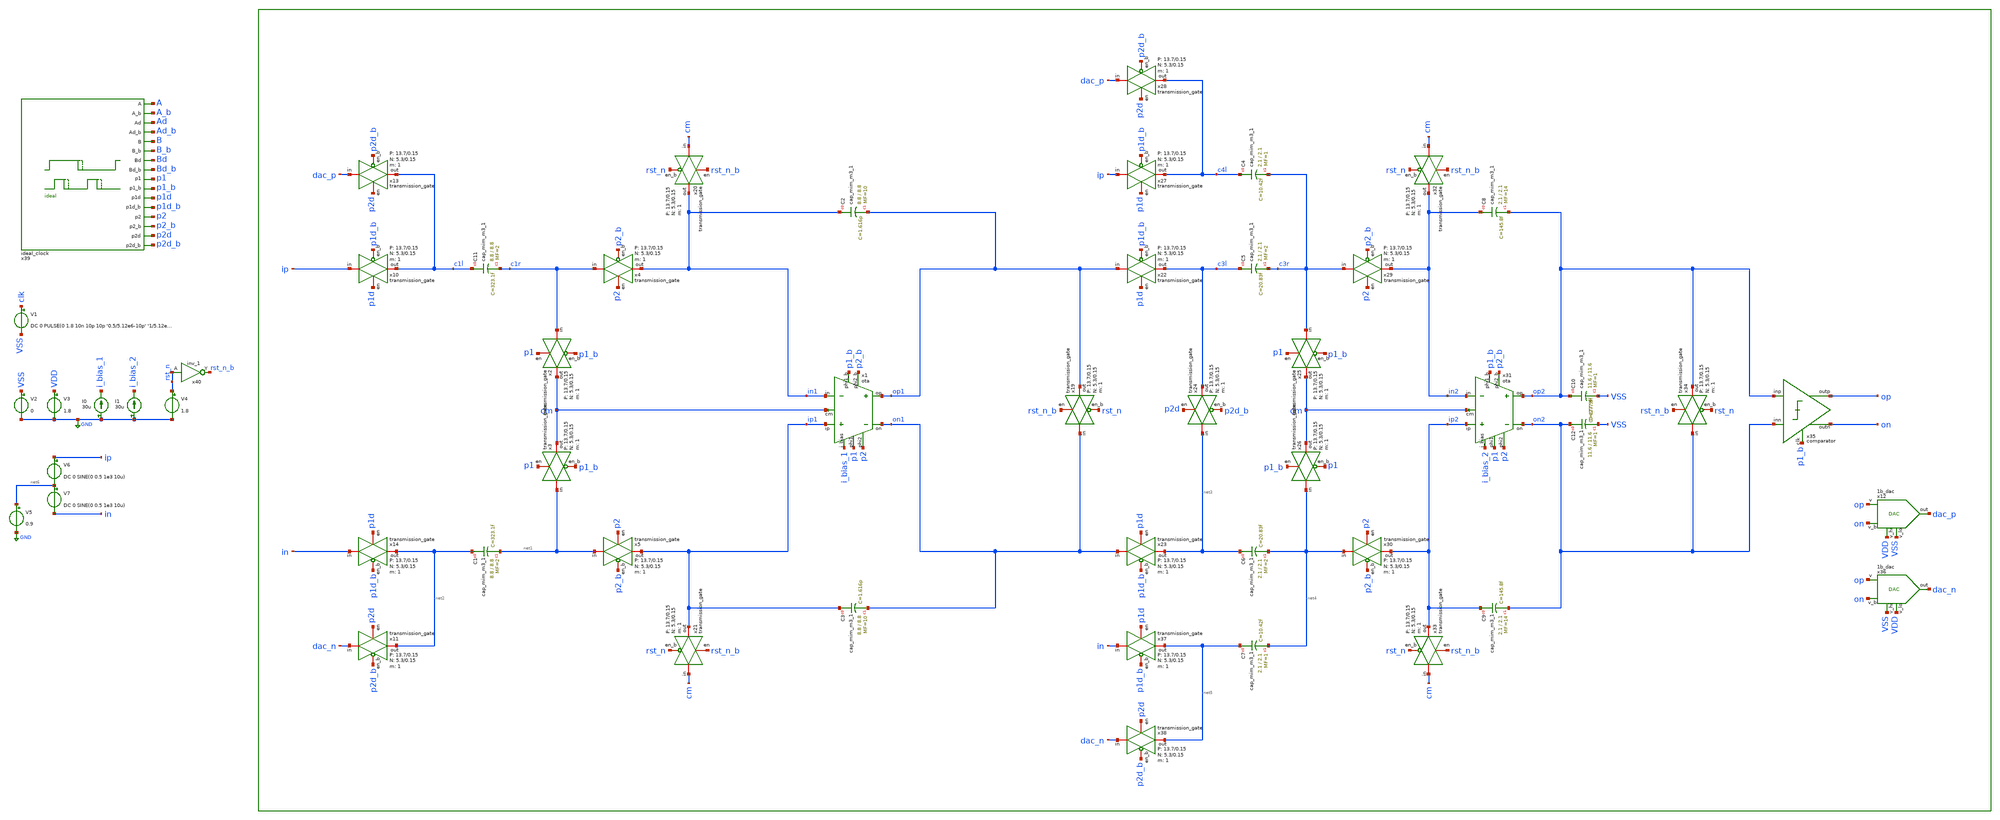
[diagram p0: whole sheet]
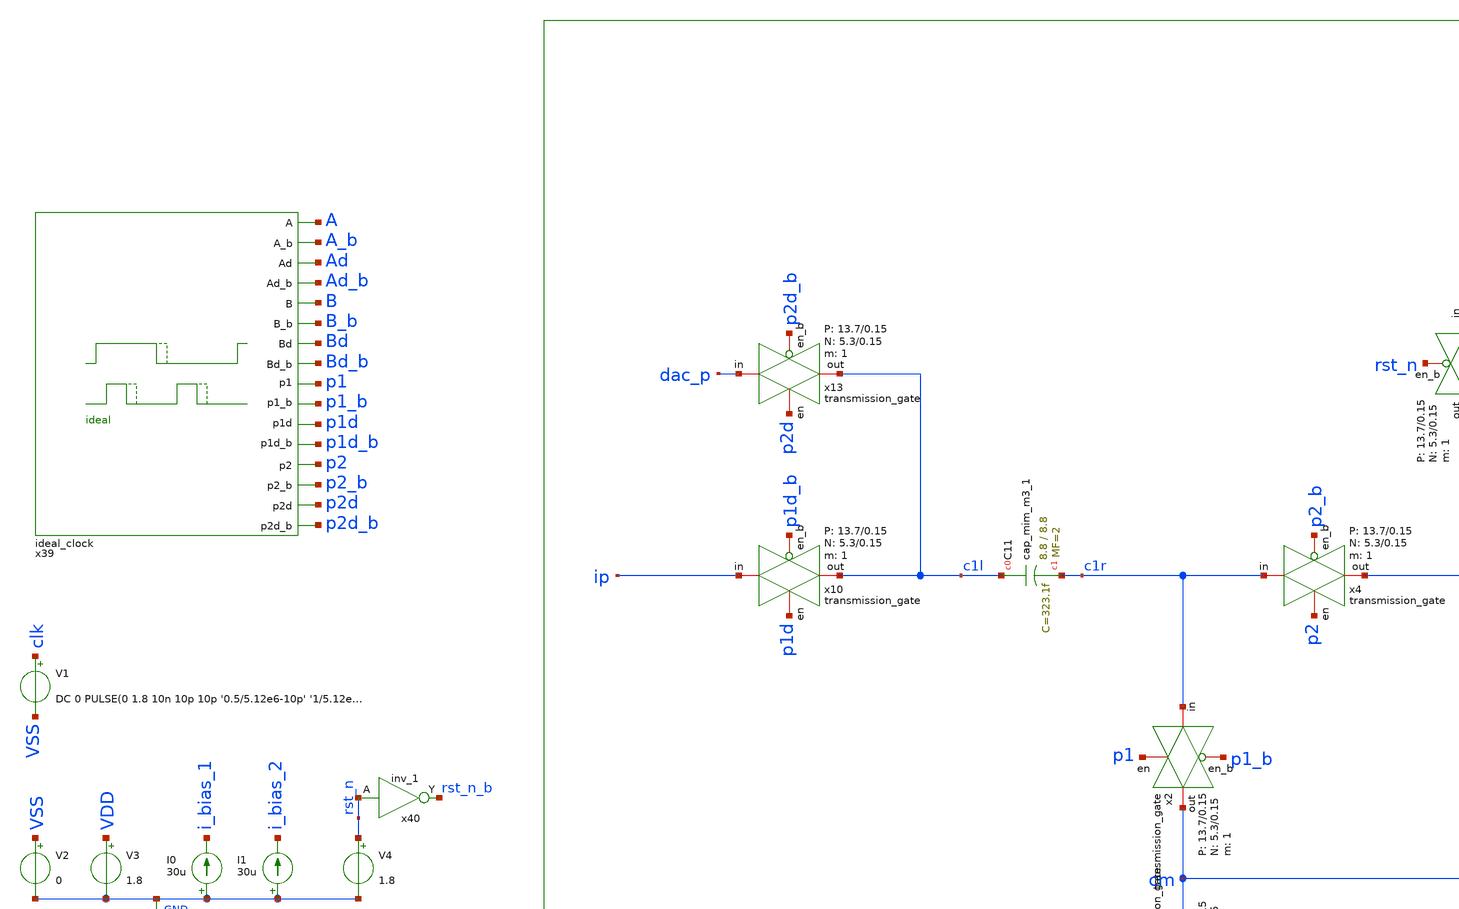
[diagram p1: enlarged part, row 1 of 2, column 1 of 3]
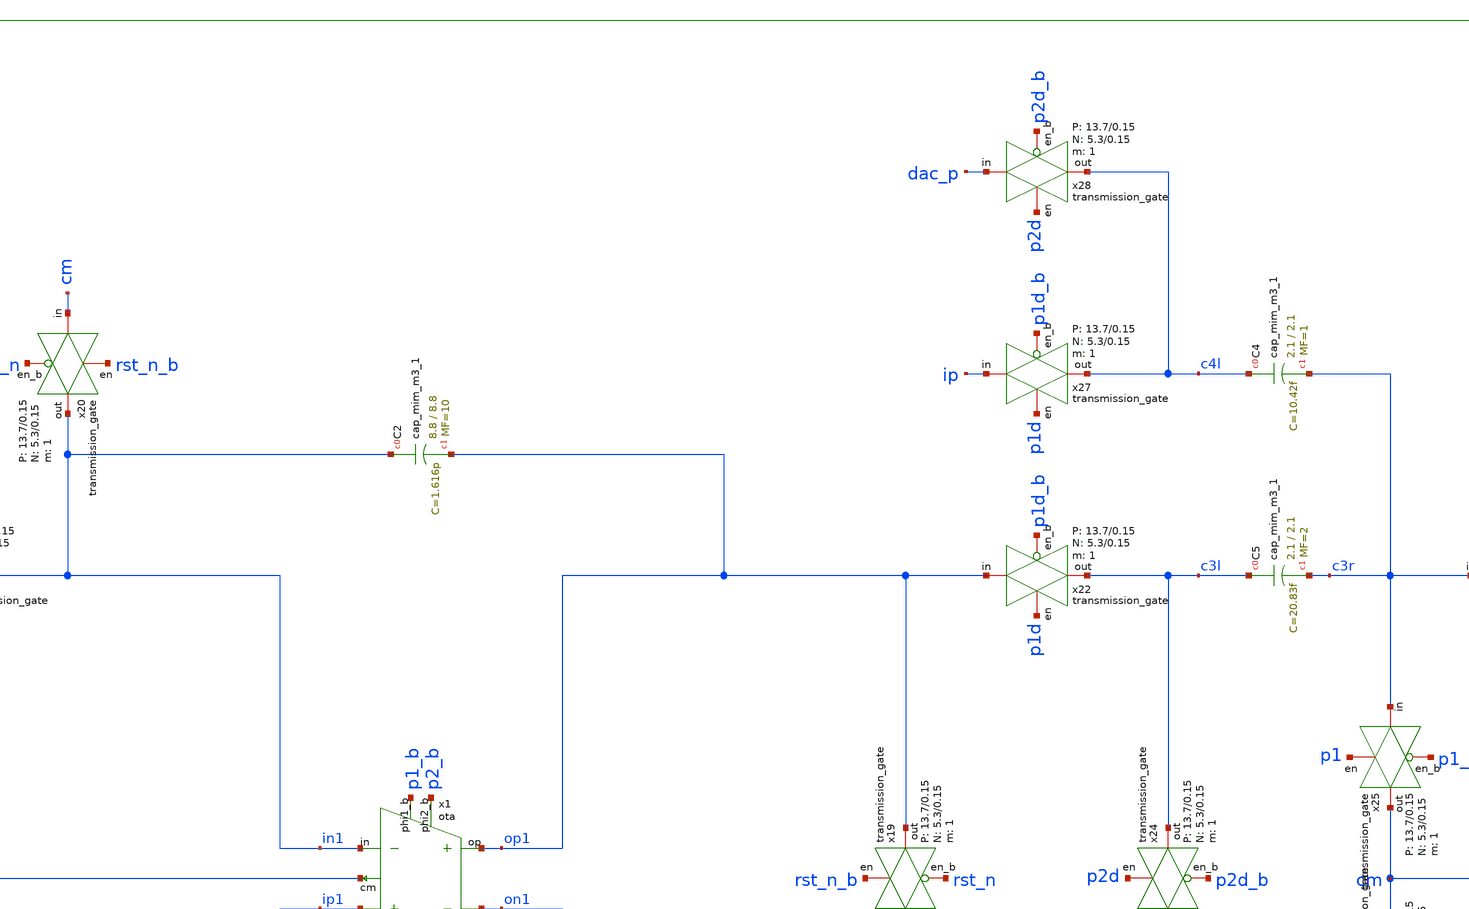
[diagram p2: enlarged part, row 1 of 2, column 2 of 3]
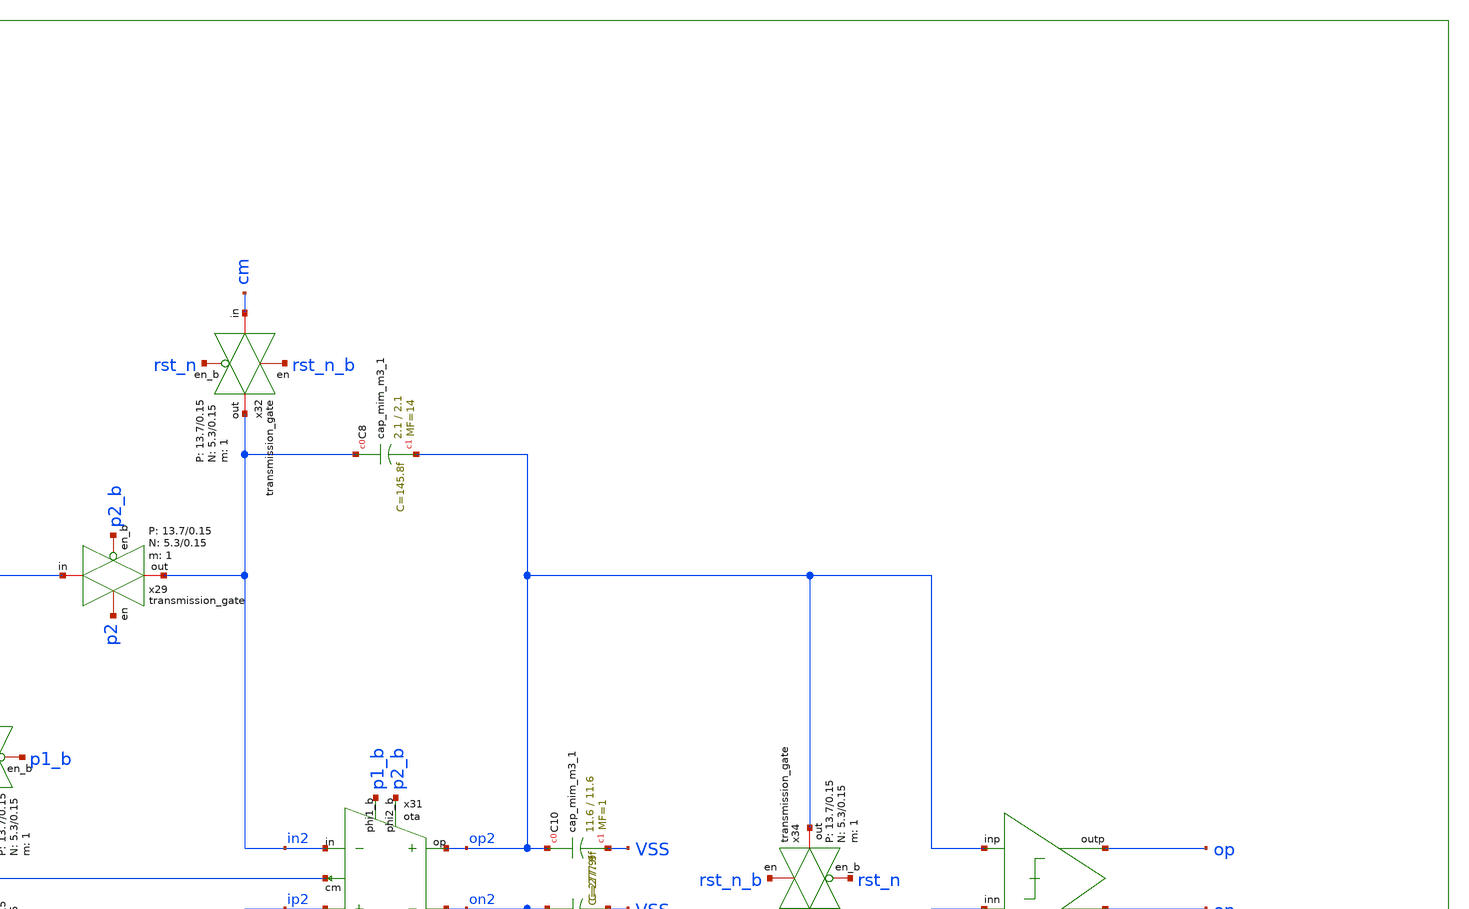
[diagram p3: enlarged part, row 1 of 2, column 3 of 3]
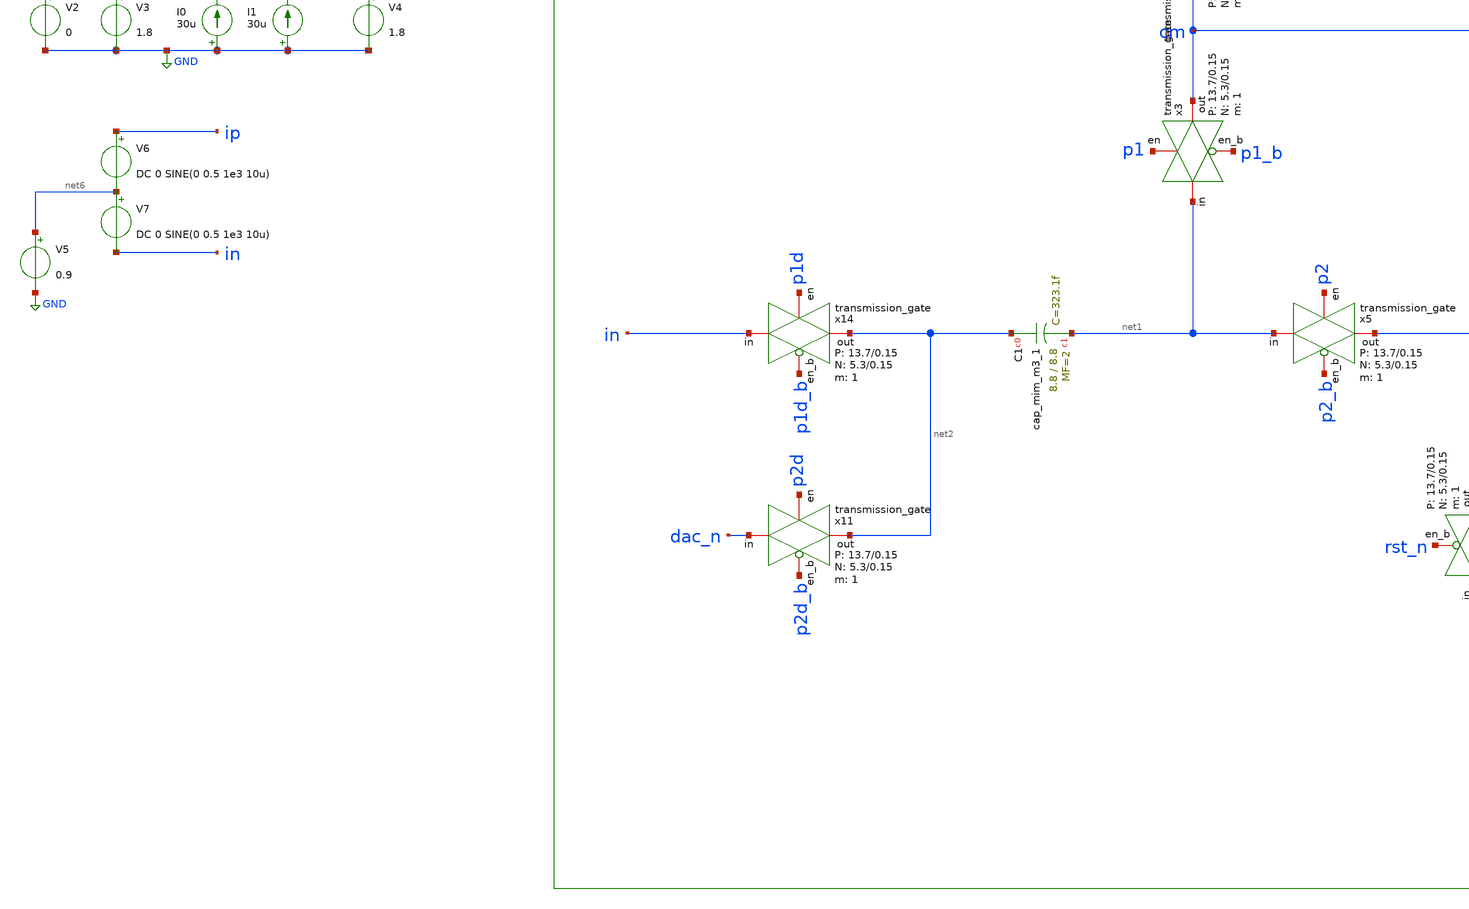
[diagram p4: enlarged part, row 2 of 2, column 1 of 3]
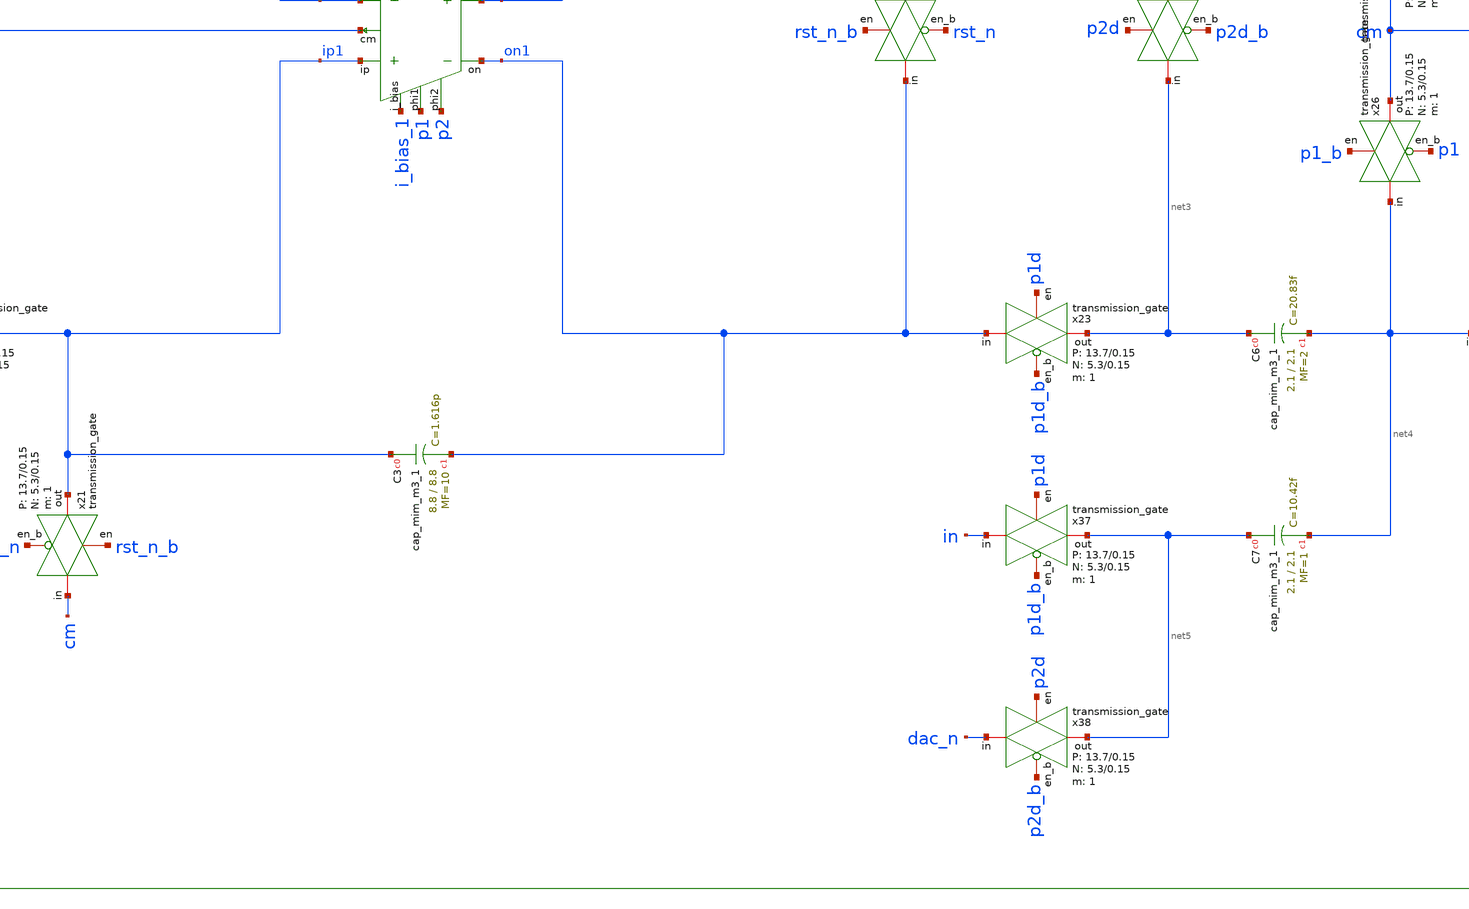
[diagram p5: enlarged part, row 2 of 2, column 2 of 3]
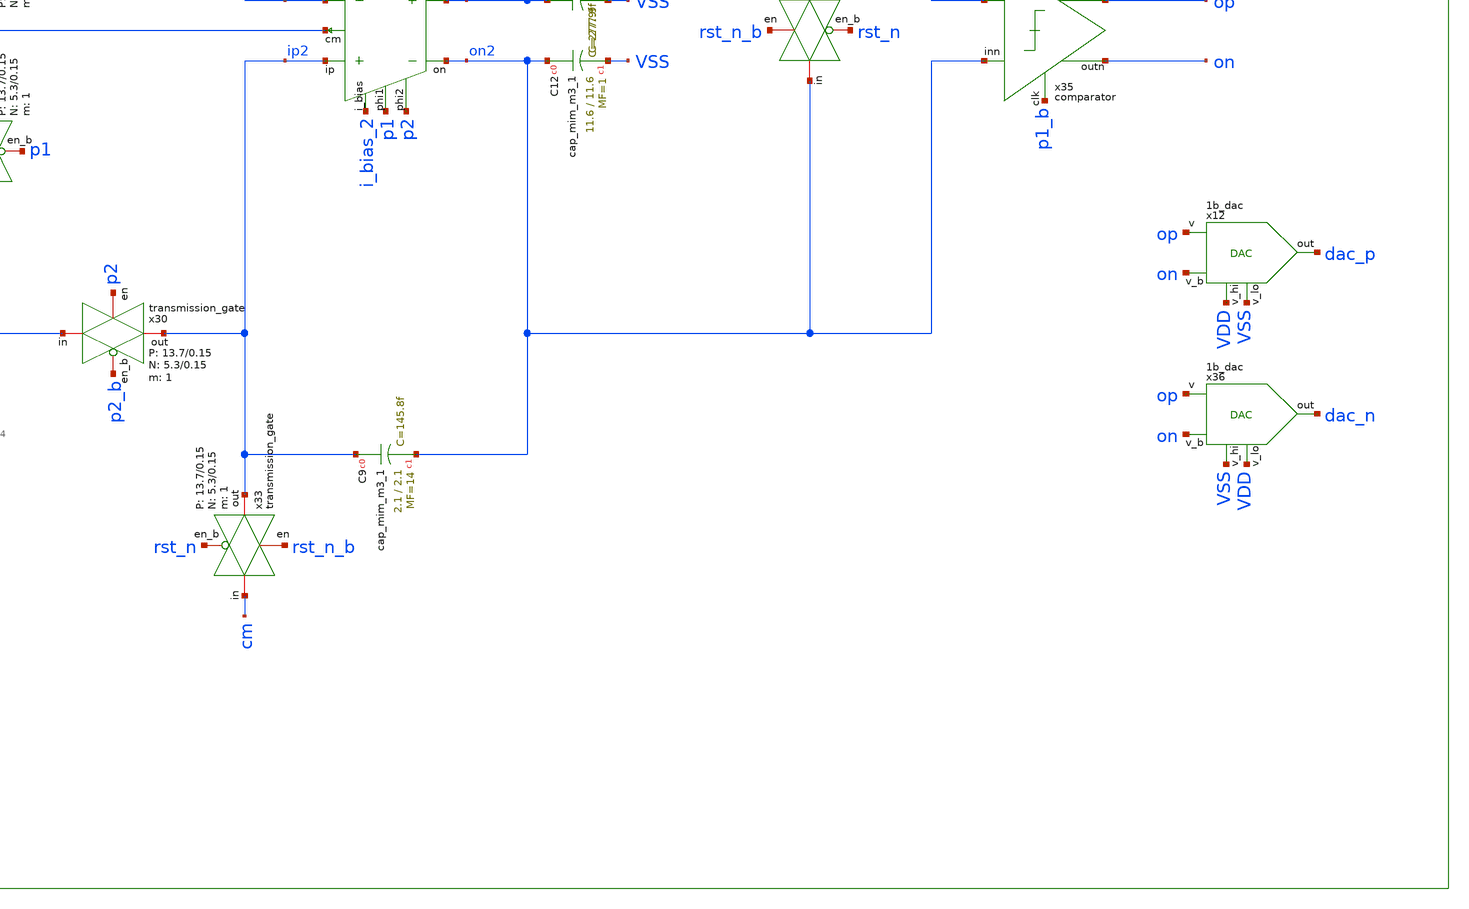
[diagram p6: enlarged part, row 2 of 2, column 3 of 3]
** sch_path: verification/schematic_sim/modulator_tb_ideal_clock_no_chopping.sch
**.subckt modulator_tb_ideal_clock_no_chopping
x1 i_bias_1 ip1 in1 p1 p1_b p2 p2_b op1 on1 cm 50 350 VDD VSS ota
x4 c1r in1 p2 p2_b VDD VSS 1 5.3 0.15 13.7 0.15 transmission_gate
x5 net1 ip1 p2 p2_b VDD VSS 1 5.3 0.15 13.7 0.15 transmission_gate
x2 c1r cm p1 p1_b VDD VSS 1 5.3 0.15 13.7 0.15 transmission_gate
x3 net1 cm p1 p1_b VDD VSS 1 5.3 0.15 13.7 0.15 transmission_gate
x10 ip c1l p1d p1d_b VDD VSS 1 5.3 0.15 13.7 0.15 transmission_gate
x11 dac_n net2 p2d p2d_b VDD VSS 1 5.3 0.15 13.7 0.15 transmission_gate
x12 VDD VSS op dac_p on VDD VSS 1b_dac
x13 dac_p c1l p2d p2d_b VDD VSS 1 5.3 0.15 13.7 0.15 transmission_gate
x14 in net2 p1d p1d_b VDD VSS 1 5.3 0.15 13.7 0.15 transmission_gate
x19 on1 op1 rst_n_b rst_n VDD VSS 1 5.3 0.15 13.7 0.15 transmission_gate
x20 cm in1 rst_n_b rst_n VDD VSS 1 5.3 0.15 13.7 0.15 transmission_gate
x21 cm ip1 rst_n_b rst_n VDD VSS 1 5.3 0.15 13.7 0.15 transmission_gate
x22 op1 c3l p1d p1d_b VDD VSS 1 5.3 0.15 13.7 0.15 transmission_gate
x23 on1 net3 p1d p1d_b VDD VSS 1 5.3 0.15 13.7 0.15 transmission_gate
x24 net3 c3l p2d p2d_b VDD VSS 1 5.3 0.15 13.7 0.15 transmission_gate
x25 c3r cm p1 p1_b VDD VSS 1 5.3 0.15 13.7 0.15 transmission_gate
x26 net4 cm p1_b p1 VDD VSS 1 5.3 0.15 13.7 0.15 transmission_gate
x27 ip c4l p1d p1d_b VDD VSS 1 5.3 0.15 13.7 0.15 transmission_gate
x28 dac_p c4l p2d p2d_b VDD VSS 1 5.3 0.15 13.7 0.15 transmission_gate
x29 c3r in2 p2 p2_b VDD VSS 1 5.3 0.15 13.7 0.15 transmission_gate
x30 net4 ip2 p2 p2_b VDD VSS 1 5.3 0.15 13.7 0.15 transmission_gate
x31 i_bias_2 ip2 in2 p1 p1_b p2 p2_b op2 on2 cm 50 350 VDD VSS ota
x32 cm in2 rst_n_b rst_n VDD VSS 1 5.3 0.15 13.7 0.15 transmission_gate
x33 cm ip2 rst_n_b rst_n VDD VSS 1 5.3 0.15 13.7 0.15 transmission_gate
x34 on2 op2 rst_n_b rst_n VDD VSS 1 5.3 0.15 13.7 0.15 transmission_gate
x35 op2 on2 op p1_b on VDD VSS comparator
x36 VSS VDD op dac_n on VDD VSS 1b_dac
x37 in net5 p1d p1d_b VDD VSS 1 5.3 0.15 13.7 0.15 transmission_gate
x38 dac_n net5 p2d p2d_b VDD VSS 1 5.3 0.15 13.7 0.15 transmission_gate
V1 clk VSS DC 0 PULSE(0 1.8 10n 10p 10p '0.5/5.12e6-10p' '1/5.12e6')
V2 VSS GND 0
V3 VDD GND 1.8
I0 GND i_bias_1 30u
I1 GND i_bias_2 30u
V4 rst_n GND 1.8
x40 rst_n GND GND VDD VDD rst_n_b sky130_fd_sc_hd__inv_1
V5 net6 GND 0.9
V6 ip net6 DC 0 SINE(0 0.5 1e3 10u)
V7 net6 in DC 0 SINE(0 0.5 1e3 10u)
XC11 c1l c1r sky130_fd_pr__cap_mim_m3_1 W=8.8 L=8.8 MF=2 m=2
XC1 net2 net1 sky130_fd_pr__cap_mim_m3_1 W=8.8 L=8.8 MF=2 m=2
XC2 in1 op1 sky130_fd_pr__cap_mim_m3_1 W=8.8 L=8.8 MF=10 m=10
XC3 ip1 on1 sky130_fd_pr__cap_mim_m3_1 W=8.8 L=8.8 MF=10 m=10
XC4 c4l c3r sky130_fd_pr__cap_mim_m3_1 W=2.1 L=2.1 MF=1 m=1
XC5 c3l c3r sky130_fd_pr__cap_mim_m3_1 W=2.1 L=2.1 MF=2 m=2
XC6 net3 net4 sky130_fd_pr__cap_mim_m3_1 W=2.1 L=2.1 MF=2 m=2
XC7 net5 net4 sky130_fd_pr__cap_mim_m3_1 W=2.1 L=2.1 MF=1 m=1
XC8 in2 op2 sky130_fd_pr__cap_mim_m3_1 W=2.1 L=2.1 MF=14 m=14
XC9 ip2 on2 sky130_fd_pr__cap_mim_m3_1 W=2.1 L=2.1 MF=14 m=14
XC10 op2 VSS sky130_fd_pr__cap_mim_m3_1 W=11.6 L=11.6 MF=1 m=1
XC12 on2 VSS sky130_fd_pr__cap_mim_m3_1 W=11.6 L=11.6 MF=1 m=1
x39 A A_b Ad Ad_b Bd_b Bd B_b B p2 p2_b p2d p2d_b p1d_b p1d p1_b p1 10u VDD VSS ideal_clock
**** begin user architecture code

** opencircuitdesign pdks install
.lib /farmshare/home/classes/ee/372/PDKs/open_pdks_1.0.310/sky130/sky130A/libs.tech/ngspice/sky130.lib.spice tt
.inc /farmshare/home/classes/ee/372/PDKs/open_pdks_1.0.310/sky130/sky130A/libs.ref/sky130_fd_sc_hd/spice/sky130_fd_sc_hd.spice



.control
tran 10n 1010u
let i_diff = v(ip) - v(in)
let vc1 = v(c1l) - v(c1r)
let i1_diff = v(ip1) - v(in1)
let o1_diff = v(op1) - v(on1)
let vc3 = v(c3l) - v(c3r)
let vc4 = v(c4l) - v(c3r)
let i2_diff = v(ip2) - v(in2)
let o2_diff = v(op2) - v(on2)
save all
write modulator_tb_ideal_clock_no_chopping.raw
.endc


**** end user architecture code
**.ends
.GLOBAL GND
.end
